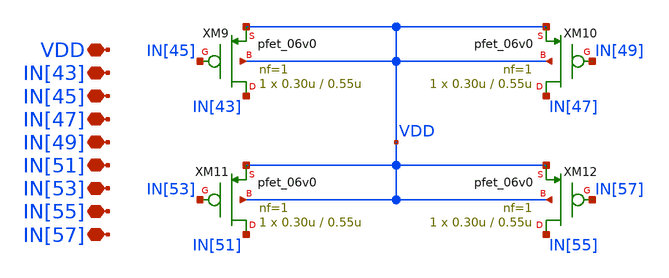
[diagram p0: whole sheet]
** sch_path: designs/libs/core_single-fet/pfet-com/pfet-com.sch
**.subckt pfet-com VDD IN[43] IN[45] IN[47] IN[49] IN[51] IN[53] IN[57] IN[55]
*.iopin VDD
*.iopin IN[43]
*.iopin IN[45]
*.iopin IN[47]
*.iopin IN[49]
*.iopin IN[51]
*.iopin IN[53]
*.iopin IN[57]
*.iopin IN[55]
XM9 IN[43] IN[45] VDD VDD pfet_06v0 L=0.55u W=0.30u nf=1 ad='int((nf+1)/2) * W/nf * 0.18u' as='int((nf+2)/2) * W/nf * 0.18u'
+ pd='2*int((nf+1)/2) * (W/nf + 0.18u)' ps='2*int((nf+2)/2) * (W/nf + 0.18u)' nrd='0.18u / W' nrs='0.18u / W'
+ sa=0 sb=0 sd=0 m=1
XM10 IN[47] IN[49] VDD VDD pfet_06v0 L=0.55u W=0.30u nf=1 ad='int((nf+1)/2) * W/nf * 0.18u' as='int((nf+2)/2) * W/nf * 0.18u'
+ pd='2*int((nf+1)/2) * (W/nf + 0.18u)' ps='2*int((nf+2)/2) * (W/nf + 0.18u)' nrd='0.18u / W' nrs='0.18u / W'
+ sa=0 sb=0 sd=0 m=1
XM11 IN[51] IN[53] VDD VDD pfet_06v0 L=0.55u W=0.30u nf=1 ad='int((nf+1)/2) * W/nf * 0.18u' as='int((nf+2)/2) * W/nf * 0.18u'
+ pd='2*int((nf+1)/2) * (W/nf + 0.18u)' ps='2*int((nf+2)/2) * (W/nf + 0.18u)' nrd='0.18u / W' nrs='0.18u / W'
+ sa=0 sb=0 sd=0 m=1
XM12 IN[55] IN[57] VDD VDD pfet_06v0 L=0.55u W=0.30u nf=1 ad='int((nf+1)/2) * W/nf * 0.18u' as='int((nf+2)/2) * W/nf * 0.18u'
+ pd='2*int((nf+1)/2) * (W/nf + 0.18u)' ps='2*int((nf+2)/2) * (W/nf + 0.18u)' nrd='0.18u / W' nrs='0.18u / W'
+ sa=0 sb=0 sd=0 m=1
**.ends
.end
